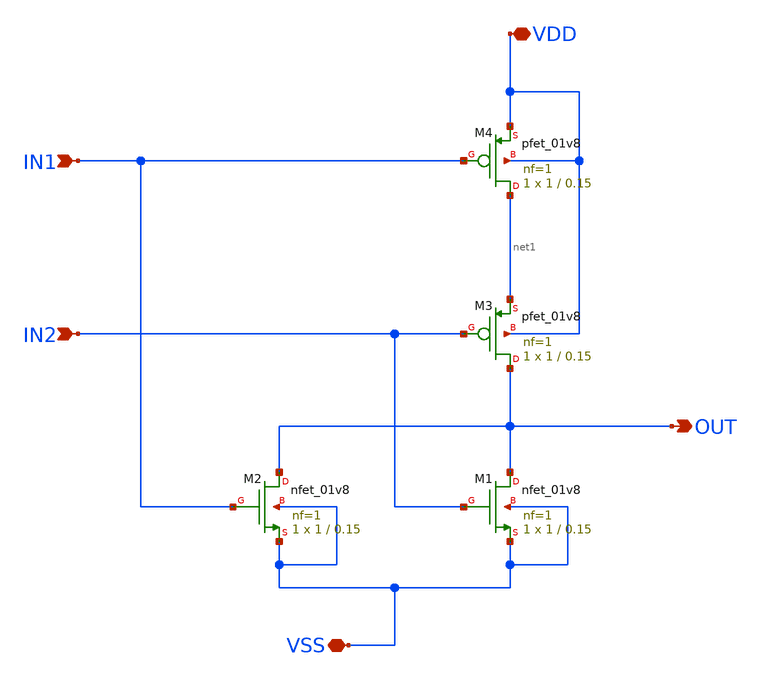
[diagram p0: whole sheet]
** sch_path: NOR/NOR.sch
**.subckt NOR VDD VSS IN1 IN2 OUT
*.iopin VDD
*.iopin VSS
*.ipin IN1
*.ipin IN2
*.opin OUT
XM1 OUT IN2 VSS VSS sky130_fd_pr__nfet_01v8 L=0.15 W=1 nf=1 ad='int((1 + 1)/2) * 1 / 1 * 0.29' as='int((1 + 2)/2) * 1 / 1 * 0.29'
+ pd='2*int((1 + 1)/2) * (1 / 1 + 0.29)' ps='2*int((1 + 2)/2) * (1 / 1 + 0.29)' nrd='0.29 / 1 ' nrs='0.29 / 1 '
+ sa=0 sb=0 sd=0 mult=1 m=1
XM2 OUT IN1 VSS VSS sky130_fd_pr__nfet_01v8 L=0.15 W=1 nf=1 ad='int((1 + 1)/2) * 1 / 1 * 0.29' as='int((1 + 2)/2) * 1 / 1 * 0.29'
+ pd='2*int((1 + 1)/2) * (1 / 1 + 0.29)' ps='2*int((1 + 2)/2) * (1 / 1 + 0.29)' nrd='0.29 / 1 ' nrs='0.29 / 1 '
+ sa=0 sb=0 sd=0 mult=1 m=1
XM3 OUT IN2 net1 VDD sky130_fd_pr__pfet_01v8 L=0.15 W=1 nf=1 ad='int((1 + 1)/2) * 1 / 1 * 0.29' as='int((1 + 2)/2) * 1 / 1 * 0.29'
+ pd='2*int((1 + 1)/2) * (1 / 1 + 0.29)' ps='2*int((1 + 2)/2) * (1 / 1 + 0.29)' nrd='0.29 / 1 ' nrs='0.29 / 1 '
+ sa=0 sb=0 sd=0 mult=1 m=1
XM4 net1 IN1 VDD VDD sky130_fd_pr__pfet_01v8 L=0.15 W=1 nf=1 ad='int((1 + 1)/2) * 1 / 1 * 0.29' as='int((1 + 2)/2) * 1 / 1 * 0.29'
+ pd='2*int((1 + 1)/2) * (1 / 1 + 0.29)' ps='2*int((1 + 2)/2) * (1 / 1 + 0.29)' nrd='0.29 / 1 ' nrs='0.29 / 1 '
+ sa=0 sb=0 sd=0 mult=1 m=1
**.ends
.end
